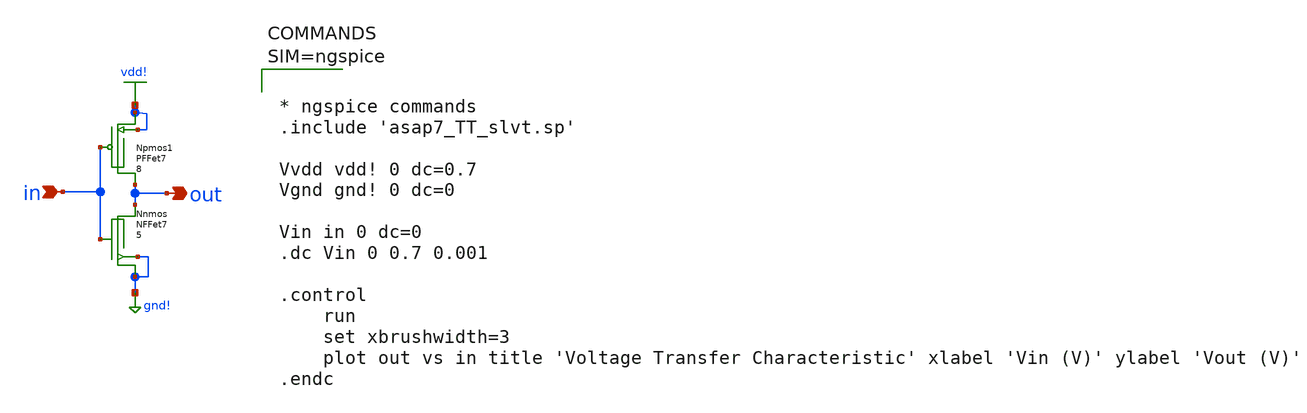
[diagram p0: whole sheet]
** sch_path: 7nm_Technology_Files/7nm_Technology_Files/Inverter1.sch
**.subckt Inverter1 in out
*.ipin in
*.opin out
Npmos1 vdd! in out vdd! BSIMCMG_osdi_P nfin=8
Nnmos gnd! in out gnd! BSIMCMG_osdi_N nfin=5
**** begin user architecture code



* ngspice commands
.include 'asap7_TT_slvt.sp'

Vvdd vdd! 0 dc=0.7
Vgnd gnd! 0 dc=0

Vin in 0 dc=0
.dc Vin 0 0.7 0.001

.control
    run
    set xbrushwidth=3
    plot out vs in title 'Voltage Transfer Characteristic' xlabel 'Vin (V)' ylabel 'Vout (V)'
.endc



**** end user architecture code
**.ends
.GLOBAL vdd!
.GLOBAL gnd!
.end
